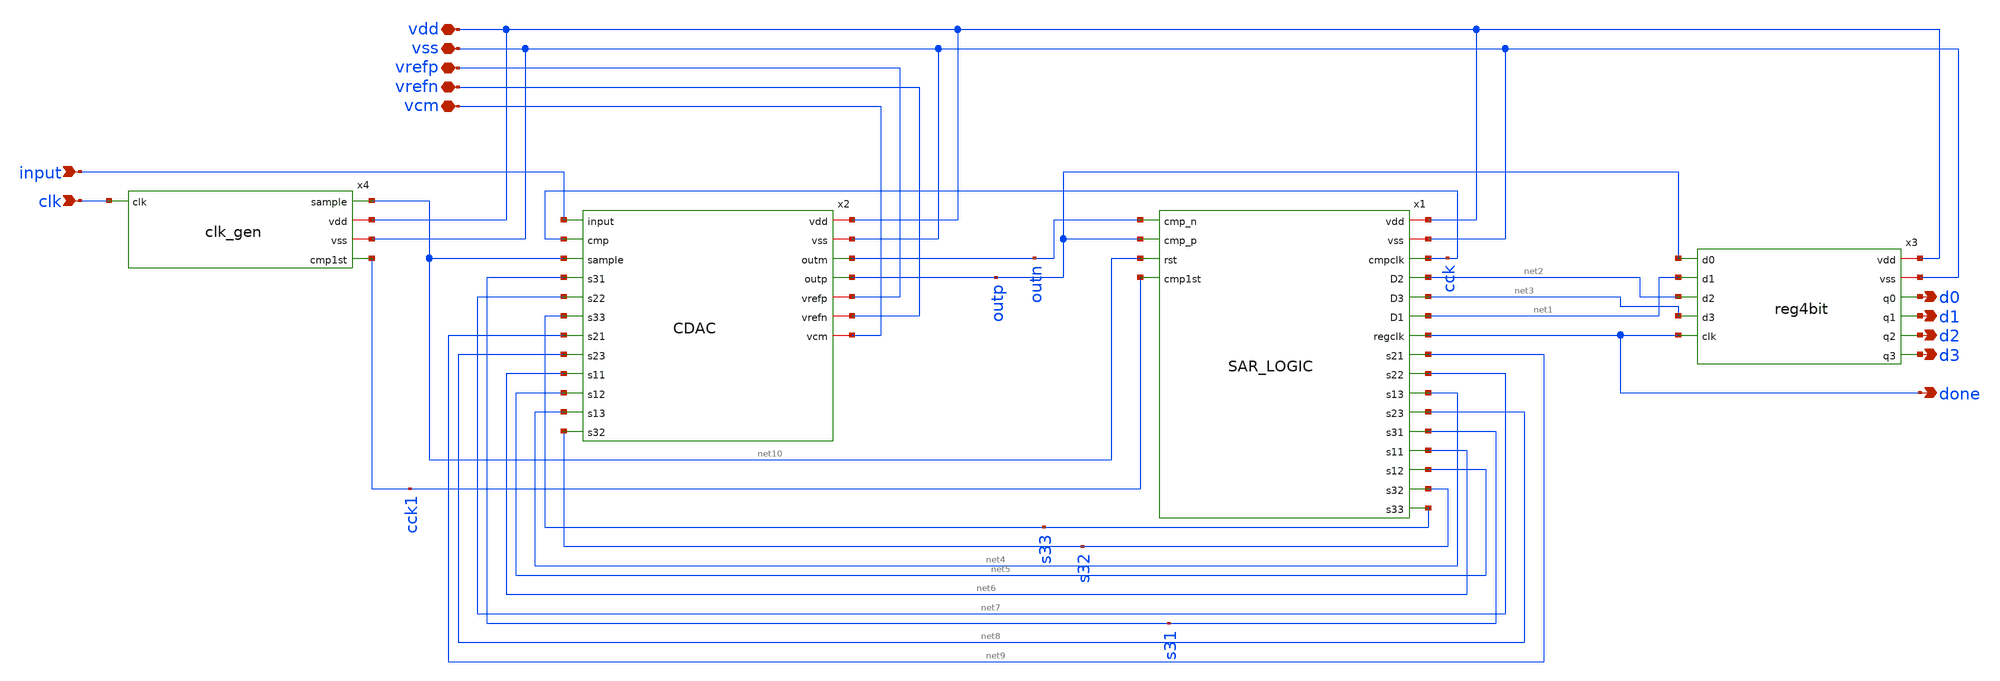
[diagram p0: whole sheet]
** sch_path: member_project/ice458/dynamic_comparator/xschem/SAR_ADC.sch
**.subckt SAR_ADC vdd vss vrefp vrefn vcm d0 d1 d2 d3 clk input done
*.iopin vdd
*.iopin vss
*.iopin vrefp
*.iopin vrefn
*.iopin vcm
*.opin d0
*.opin d1
*.opin d2
*.opin d3
*.ipin clk
*.ipin input
*.opin done
x1 vdd vss outn outp net10 cck1 cck net2 net3 net1 done net9 net7 net4 net8 s31 net6 net5 s32 s33
+ SAR_LOGIC
x2 vdd vss input outn outp cck net10 s31 net7 s33 net9 net8 net6 net5 net4 s32 vrefp vrefn vcm CDAC
x3 vdd vss d0 outp d1 net1 d2 net2 d3 net3 done reg4bit
x4 net10 vdd vss clk cck1 clk_gen
**.ends
.end
